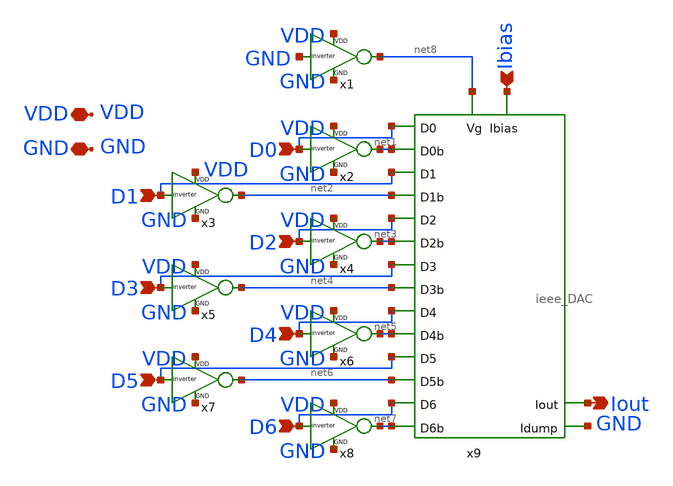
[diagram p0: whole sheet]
** sch_path: schematics/ieee_simple_M_2M_DAC.sch
**.subckt ieee_simple_M_2M_DAC Ibias Iout D0 D1 D2 D3 D4 D5 D6 VDD GND
*.ipin Ibias
*.opin Iout
*.ipin D0
*.ipin D1
*.ipin D2
*.ipin D3
*.ipin D4
*.ipin D5
*.ipin D6
*.iopin VDD
*.iopin GND
x2 VDD D0 net1 GND inverter
x3 VDD D1 net2 GND inverter
x4 VDD D2 net3 GND inverter
x5 VDD D3 net4 GND inverter
x6 VDD D4 net5 GND inverter
x7 VDD D5 net6 GND inverter
x8 VDD D6 net7 GND inverter
x9 Ibias net8 D0 D2 D3 D4 D5 net6 D1 net1 net2 net3 net4 net5 D6 net7 Iout GND ieee_DAC
x1 VDD GND net8 GND inverter
**.ends
.end
